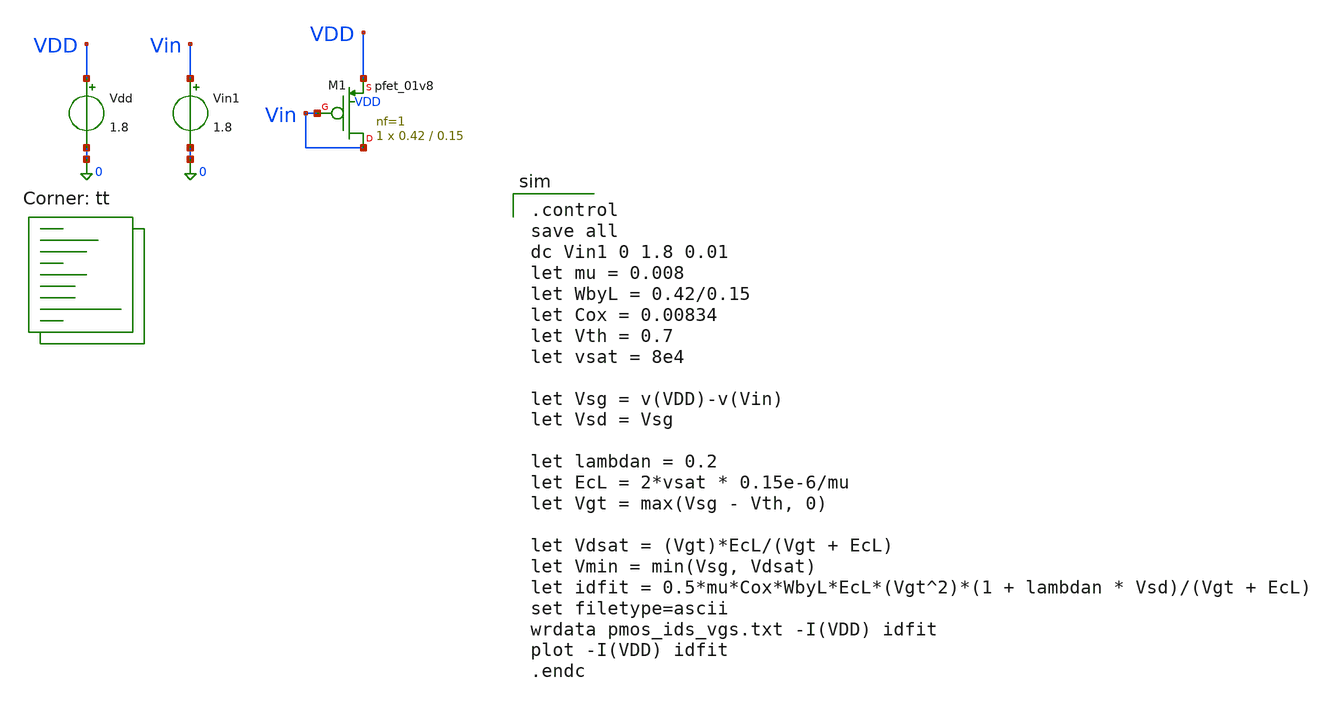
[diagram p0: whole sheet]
** sch_path: tutorial-1/source/q2a.sch
**.subckt q2a
XM1 Vin Vin VDD VDD sky130_fd_pr__pfet_01v8 L=0.15 W=0.42 nf=1 ad='int((nf+1)/2) * W/nf * 0.29' as='int((nf+2)/2) * W/nf * 0.29'
+ pd='2*int((nf+1)/2) * (W/nf + 0.29)' ps='2*int((nf+2)/2) * (W/nf + 0.29)' nrd='0.29 / W' nrs='0.29 / W'
+ sa=0 sb=0 sd=0 mult=1 m=1
Vin1 Vin 0 1.8
Vdd VDD 0 1.8
**** begin user architecture code
.lib $::SKYWATER_MODELS/sky130.lib.spice tt

.control
save all
dc Vin1 0 1.8 0.01
let mu = 0.008
let WbyL = 0.42/0.15
let Cox = 0.00834
let Vth = 0.7
let vsat = 8e4

let Vsg = v(VDD)-v(Vin)
let Vsd = Vsg

let lambdan = 0.2
let EcL = 2*vsat * 0.15e-6/mu
let Vgt = max(Vsg - Vth, 0)

let Vdsat = (Vgt)*EcL/(Vgt + EcL)
let Vmin = min(Vsg, Vdsat)
let idfit = 0.5*mu*Cox*WbyL*EcL*(Vgt^2)*(1 + lambdan * Vsd)/(Vgt + EcL)
set filetype=ascii
wrdata pmos_ids_vgs.txt -I(VDD) idfit
plot -I(VDD) idfit
.endc

**** end user architecture code
**.ends
.end
